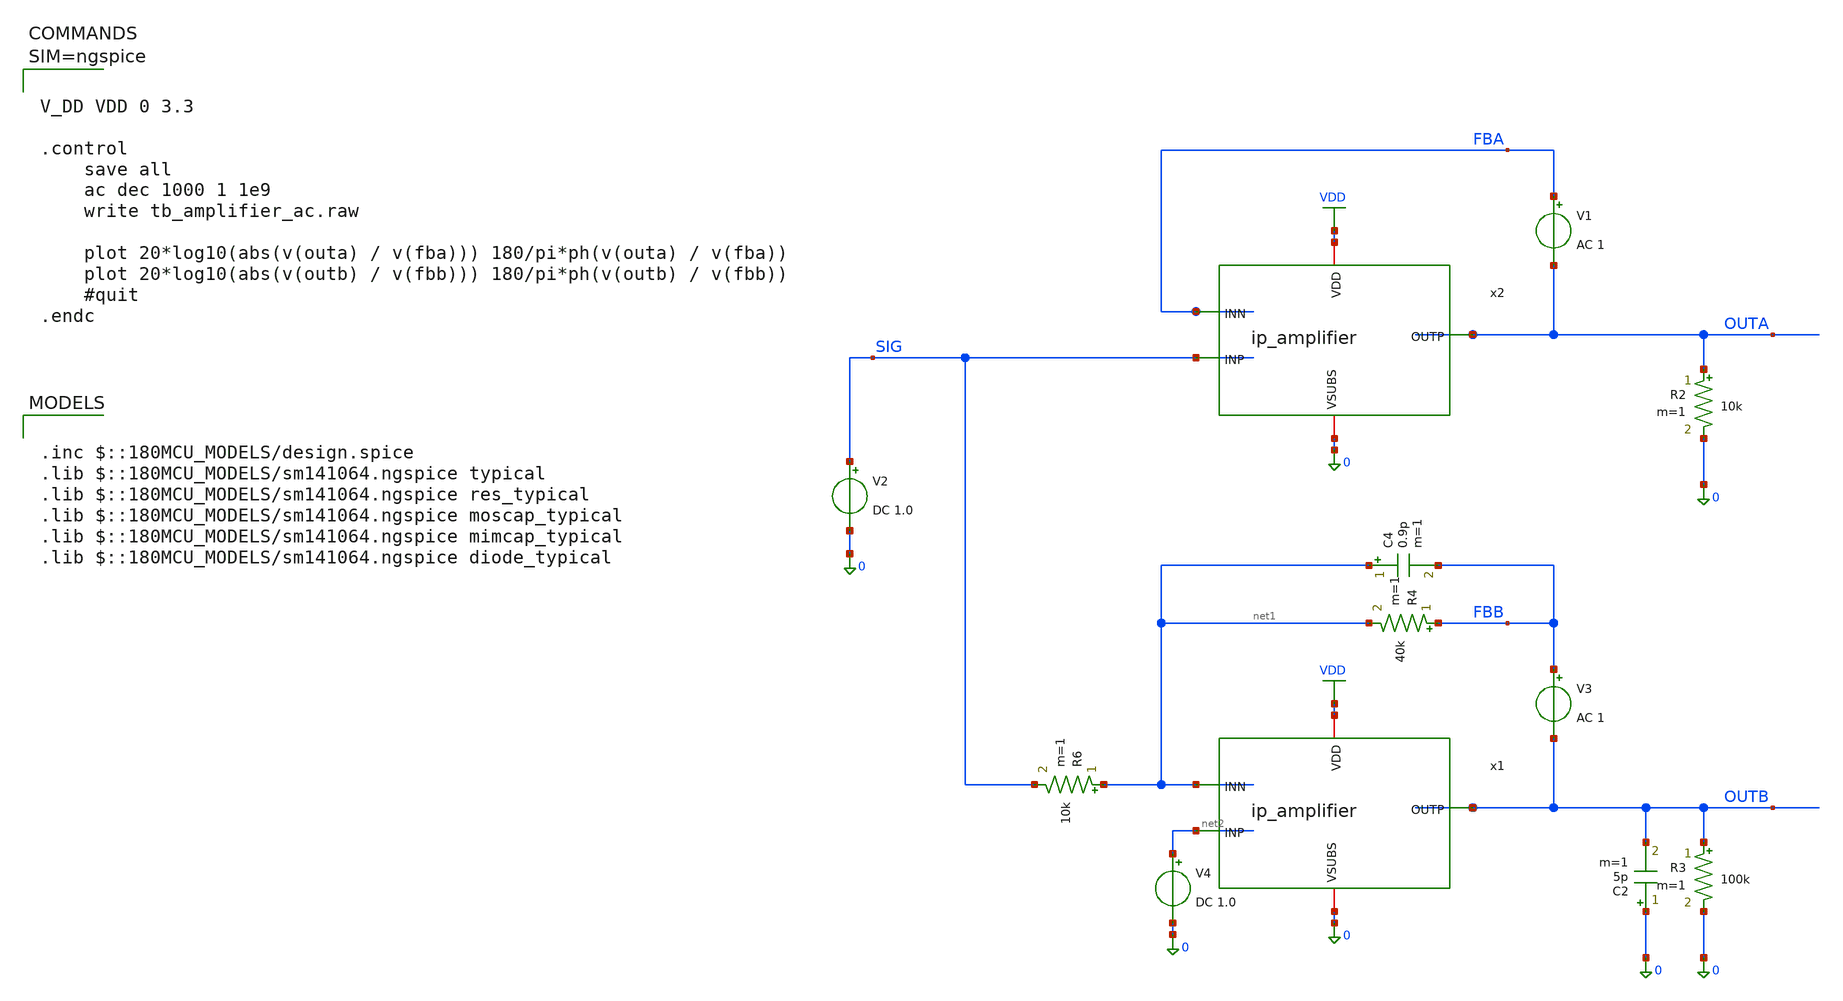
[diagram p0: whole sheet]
** sch_path: xschem/tb_amplifier_ac.sch
**.subckt tb_amplifier_ac
V2 SIG 0 DC 1.0
x2 VDD OUTA SIG FBA 0 ip_amplifier
R2 OUTA 0 10k m=1
V1 FBA OUTA AC 1
x1 VDD OUTB net2 net1 0 ip_amplifier
R3 OUTB 0 100k m=1
V3 FBB OUTB AC 1
R4 FBB net1 40k m=1
R6 net1 SIG 10k m=1
V4 net2 0 DC 1.0
C2 0 OUTB 5p m=1
C4 net1 FBB 0.9p m=1
**** begin user architecture code

.inc $::180MCU_MODELS/design.spice
.lib $::180MCU_MODELS/sm141064.ngspice typical
.lib $::180MCU_MODELS/sm141064.ngspice res_typical
.lib $::180MCU_MODELS/sm141064.ngspice moscap_typical
.lib $::180MCU_MODELS/sm141064.ngspice mimcap_typical
.lib $::180MCU_MODELS/sm141064.ngspice diode_typical




V_DD VDD 0 3.3

.control
	save all
	ac dec 1000 1 1e9
	write tb_amplifier_ac.raw

	plot 20*log10(abs(v(outa) / v(fba))) 180/pi*ph(v(outa) / v(fba))
	plot 20*log10(abs(v(outb) / v(fbb))) 180/pi*ph(v(outb) / v(fbb))
	#quit
.endc



**** end user architecture code
**.ends

* expanding   symbol:  ip_amplifier.sym # of pins=5
** sym_path: xschem/ip_amplifier.sym
** sch_path: xschem/ip_amplifier.sch
.subckt ip_amplifier VDD OUTP INP INN VSUBS
*.iopin VDD
*.iopin VSUBS
*.ipin INP
*.ipin INN
*.opin OUTP
XM1 net10 INP net8 VDD pfet_06v0 L=0.7u W=7.0u nf=1 ad='int((nf+1)/2) * W/nf * 0.18u' as='int((nf+2)/2) * W/nf * 0.18u'
+ pd='2*int((nf+1)/2) * (W/nf + 0.18u)' ps='2*int((nf+2)/2) * (W/nf + 0.18u)' nrd='0.18u / W' nrs='0.18u / W'
+ sa=0 sb=0 sd=0 m=3 par=3
XM2 net9 INN net8 VDD pfet_06v0 L=0.7u W=7.0u nf=1 ad='int((nf+1)/2) * W/nf * 0.18u' as='int((nf+2)/2) * W/nf * 0.18u'
+ pd='2*int((nf+1)/2) * (W/nf + 0.18u)' ps='2*int((nf+2)/2) * (W/nf + 0.18u)' nrd='0.18u / W' nrs='0.18u / W'
+ sa=0 sb=0 sd=0 m=3 par=3
XM5 net10 net1 VSUBS vsubs nfet_06v0 L=2u W=5u nf=1 ad='int((nf+1)/2) * W/nf * 0.18u' as='int((nf+2)/2) * W/nf * 0.18u'
+ pd='2*int((nf+1)/2) * (W/nf + 0.18u)' ps='2*int((nf+2)/2) * (W/nf + 0.18u)' nrd='0.18u / W' nrs='0.18u / W'
+ sa=0 sb=0 sd=0 m=1 par=1
XM6 net9 net1 VSUBS vsubs nfet_06v0 L=2u W=5u nf=1 ad='int((nf+1)/2) * W/nf * 0.18u' as='int((nf+2)/2) * W/nf * 0.18u'
+ pd='2*int((nf+1)/2) * (W/nf + 0.18u)' ps='2*int((nf+2)/2) * (W/nf + 0.18u)' nrd='0.18u / W' nrs='0.18u / W'
+ sa=0 sb=0 sd=0 m=1 par=1
XM3 net3 net1 VSUBS vsubs nfet_06v0 L=1u W=5u nf=1 ad='int((nf+1)/2) * W/nf * 0.18u' as='int((nf+2)/2) * W/nf * 0.18u'
+ pd='2*int((nf+1)/2) * (W/nf + 0.18u)' ps='2*int((nf+2)/2) * (W/nf + 0.18u)' nrd='0.18u / W' nrs='0.18u / W'
+ sa=0 sb=0 sd=0 m=5 par=5
XM4 net2 net1 VSUBS vsubs nfet_06v0 L=1u W=5u nf=1 ad='int((nf+1)/2) * W/nf * 0.18u' as='int((nf+2)/2) * W/nf * 0.18u'
+ pd='2*int((nf+1)/2) * (W/nf + 0.18u)' ps='2*int((nf+2)/2) * (W/nf + 0.18u)' nrd='0.18u / W' nrs='0.18u / W'
+ sa=0 sb=0 sd=0 m=1 par=1
XM7 net1 net1 net3 vsubs nfet_06v0 L=0.7u W=5u nf=1 ad='int((nf+1)/2) * W/nf * 0.18u' as='int((nf+2)/2) * W/nf * 0.18u'
+ pd='2*int((nf+1)/2) * (W/nf + 0.18u)' ps='2*int((nf+2)/2) * (W/nf + 0.18u)' nrd='0.18u / W' nrs='0.18u / W'
+ sa=0 sb=0 sd=0 m=7 par=7
XM8 net4 net1 net2 vsubs nfet_06v0 L=0.7u W=5u nf=1 ad='int((nf+1)/2) * W/nf * 0.18u' as='int((nf+2)/2) * W/nf * 0.18u'
+ pd='2*int((nf+1)/2) * (W/nf + 0.18u)' ps='2*int((nf+2)/2) * (W/nf + 0.18u)' nrd='0.18u / W' nrs='0.18u / W'
+ sa=0 sb=0 sd=0 m=7 par=7
XM9 net5 net7 VDD VDD pfet_06v0 L=1u W=6u nf=1 ad='int((nf+1)/2) * W/nf * 0.18u' as='int((nf+2)/2) * W/nf * 0.18u'
+ pd='2*int((nf+1)/2) * (W/nf + 0.18u)' ps='2*int((nf+2)/2) * (W/nf + 0.18u)' nrd='0.18u / W' nrs='0.18u / W'
+ sa=0 sb=0 sd=0 m=1 par=1
XM10 net6 net7 VDD VDD pfet_06v0 L=1u W=6u nf=1 ad='int((nf+1)/2) * W/nf * 0.18u' as='int((nf+2)/2) * W/nf * 0.18u'
+ pd='2*int((nf+1)/2) * (W/nf + 0.18u)' ps='2*int((nf+2)/2) * (W/nf + 0.18u)' nrd='0.18u / W' nrs='0.18u / W'
+ sa=0 sb=0 sd=0 m=1 par=1
XM11 net7 net7 net5 VDD pfet_06v0 L=0.7u W=7u nf=1 ad='int((nf+1)/2) * W/nf * 0.18u' as='int((nf+2)/2) * W/nf * 0.18u'
+ pd='2*int((nf+1)/2) * (W/nf + 0.18u)' ps='2*int((nf+2)/2) * (W/nf + 0.18u)' nrd='0.18u / W' nrs='0.18u / W'
+ sa=0 sb=0 sd=0 m=5 par=5
XM12 net8 net7 net6 VDD pfet_06v0 L=0.7u W=7u nf=1 ad='int((nf+1)/2) * W/nf * 0.18u' as='int((nf+2)/2) * W/nf * 0.18u'
+ pd='2*int((nf+1)/2) * (W/nf + 0.18u)' ps='2*int((nf+2)/2) * (W/nf + 0.18u)' nrd='0.18u / W' nrs='0.18u / W'
+ sa=0 sb=0 sd=0 m=5 par=5
XM13 net11 net1 net9 vsubs nfet_06v0 L=0.7u W=7u nf=1 ad='int((nf+1)/2) * W/nf * 0.18u' as='int((nf+2)/2) * W/nf * 0.18u'
+ pd='2*int((nf+1)/2) * (W/nf + 0.18u)' ps='2*int((nf+2)/2) * (W/nf + 0.18u)' nrd='0.18u / W' nrs='0.18u / W'
+ sa=0 sb=0 sd=0 m=1 par=1
XM14 COMP net1 net10 vsubs nfet_06v0 L=0.7u W=7u nf=1 ad='int((nf+1)/2) * W/nf * 0.18u' as='int((nf+2)/2) * W/nf * 0.18u'
+ pd='2*int((nf+1)/2) * (W/nf + 0.18u)' ps='2*int((nf+2)/2) * (W/nf + 0.18u)' nrd='0.18u / W' nrs='0.18u / W'
+ sa=0 sb=0 sd=0 m=1 par=1
XM15 net11 net11 VDD VDD pfet_06v0 L=0.7u W=7u nf=1 ad='int((nf+1)/2) * W/nf * 0.18u' as='int((nf+2)/2) * W/nf * 0.18u'
+ pd='2*int((nf+1)/2) * (W/nf + 0.18u)' ps='2*int((nf+2)/2) * (W/nf + 0.18u)' nrd='0.18u / W' nrs='0.18u / W'
+ sa=0 sb=0 sd=0 m=1 par=1
XM16 COMP net11 VDD VDD pfet_06v0 L=0.7u W=7u nf=1 ad='int((nf+1)/2) * W/nf * 0.18u' as='int((nf+2)/2) * W/nf * 0.18u'
+ pd='2*int((nf+1)/2) * (W/nf + 0.18u)' ps='2*int((nf+2)/2) * (W/nf + 0.18u)' nrd='0.18u / W' nrs='0.18u / W'
+ sa=0 sb=0 sd=0 m=1 par=1
XM17 OUTP COMP VDD VDD pfet_06v0 L=0.5u W=5u nf=1 ad='int((nf+1)/2) * W/nf * 0.18u' as='int((nf+2)/2) * W/nf * 0.18u'
+ pd='2*int((nf+1)/2) * (W/nf + 0.18u)' ps='2*int((nf+2)/2) * (W/nf + 0.18u)' nrd='0.18u / W' nrs='0.18u / W'
+ sa=0 sb=0 sd=0 m=12 par=12
XM18 OUTP net10 VSUBS vsubs nfet_06v0 L=0.7u W=5u nf=1 ad='int((nf+1)/2) * W/nf * 0.18u' as='int((nf+2)/2) * W/nf * 0.18u'
+ pd='2*int((nf+1)/2) * (W/nf + 0.18u)' ps='2*int((nf+2)/2) * (W/nf + 0.18u)' nrd='0.18u / W' nrs='0.18u / W'
+ sa=0 sb=0 sd=0 m=6 par=6
XR3 net1 net14 vsubs ppolyf_u_1k_6p0 r_width=1e-6 r_length=6e-6 m=1
XR6 net14 net13 vsubs ppolyf_u_1k_6p0 r_width=1e-6 r_length=6e-6 m=1
XR7 net13 net12 vsubs ppolyf_u_1k_6p0 r_width=1e-6 r_length=6e-6 m=1
XR8 net12 net15 vsubs ppolyf_u_1k_6p0 r_width=1e-6 r_length=4e-6 m=1
Vmeas VDD net15 0
Vmeas1 net7 net4 0
XC1 OUTP net16 cap_nmos_03v3 c_width=12e-6 c_length=18e-6 m=1
XC2 COMP net19 cap_nmos_03v3 c_width=12e-6 c_length=18e-6 m=1
XR12 net16 net17 vsubs ppolyf_u_1k_6p0 r_width=1e-6 r_length=5e-6 m=1
XR13 net17 COMP vsubs ppolyf_u_1k_6p0 r_width=1e-6 r_length=5e-6 m=1
XR15 OUTP net18 vsubs ppolyf_u_1k_6p0 r_width=1e-6 r_length=5e-6 m=1
XR16 net18 net19 vsubs ppolyf_u_1k_6p0 r_width=1e-6 r_length=5e-6 m=1
.ends

.GLOBAL VDD
.end
